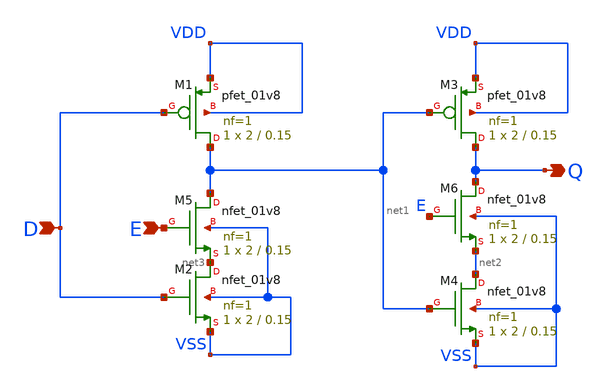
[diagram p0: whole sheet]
** sch_path: xschem/attic/TSPC_Latch.sch
**.subckt TSPC_Latch D E Q
*.ipin D
*.ipin E
*.opin Q
XM1 net1 D VDD VDD sky130_fd_pr__pfet_01v8 L=0.15 W=2 nf=1 ad='int((nf+1)/2) * W/nf * 0.29' as='int((nf+2)/2) * W/nf * 0.29'
+ pd='2*int((nf+1)/2) * (W/nf + 0.29)' ps='2*int((nf+2)/2) * (W/nf + 0.29)' nrd='0.29 / W' nrs='0.29 / W'
+ sa=0 sb=0 sd=0 mult=1 m=1
XM2 net3 D VSS VSS sky130_fd_pr__nfet_01v8 L=0.15 W=2 nf=1 ad='int((nf+1)/2) * W/nf * 0.29' as='int((nf+2)/2) * W/nf * 0.29'
+ pd='2*int((nf+1)/2) * (W/nf + 0.29)' ps='2*int((nf+2)/2) * (W/nf + 0.29)' nrd='0.29 / W' nrs='0.29 / W'
+ sa=0 sb=0 sd=0 mult=1 m=1
XM3 Q net1 VDD VDD sky130_fd_pr__pfet_01v8 L=0.15 W=2 nf=1 ad='int((nf+1)/2) * W/nf * 0.29' as='int((nf+2)/2) * W/nf * 0.29'
+ pd='2*int((nf+1)/2) * (W/nf + 0.29)' ps='2*int((nf+2)/2) * (W/nf + 0.29)' nrd='0.29 / W' nrs='0.29 / W'
+ sa=0 sb=0 sd=0 mult=1 m=1
XM4 net2 net1 VSS VSS sky130_fd_pr__nfet_01v8 L=0.15 W=2 nf=1 ad='int((nf+1)/2) * W/nf * 0.29' as='int((nf+2)/2) * W/nf * 0.29'
+ pd='2*int((nf+1)/2) * (W/nf + 0.29)' ps='2*int((nf+2)/2) * (W/nf + 0.29)' nrd='0.29 / W' nrs='0.29 / W'
+ sa=0 sb=0 sd=0 mult=1 m=1
XM5 net1 E net3 VSS sky130_fd_pr__nfet_01v8 L=0.15 W=2 nf=1 ad='int((nf+1)/2) * W/nf * 0.29' as='int((nf+2)/2) * W/nf * 0.29'
+ pd='2*int((nf+1)/2) * (W/nf + 0.29)' ps='2*int((nf+2)/2) * (W/nf + 0.29)' nrd='0.29 / W' nrs='0.29 / W'
+ sa=0 sb=0 sd=0 mult=1 m=1
XM6 Q E net2 VSS sky130_fd_pr__nfet_01v8 L=0.15 W=2 nf=1 ad='int((nf+1)/2) * W/nf * 0.29' as='int((nf+2)/2) * W/nf * 0.29'
+ pd='2*int((nf+1)/2) * (W/nf + 0.29)' ps='2*int((nf+2)/2) * (W/nf + 0.29)' nrd='0.29 / W' nrs='0.29 / W'
+ sa=0 sb=0 sd=0 mult=1 m=1
**.ends
.end
